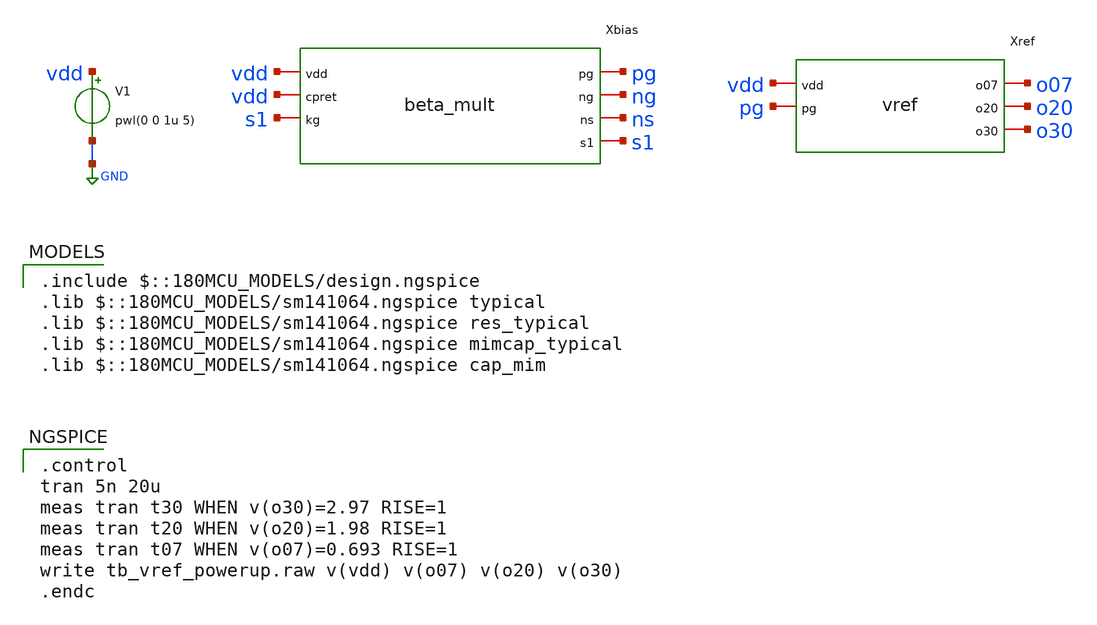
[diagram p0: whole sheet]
** sch_path: schematic pt2/sims/tb/tb_vref_powerup.sch
**.subckt tb_vref_powerup
V1 vdd GND pwl(0 0 1u 5)
Xbias vdd pg ng ns vdd s1 s1 beta_mult
Xref vdd pg o07 o20 o30 vref
**** begin user architecture code
 .include $::180MCU_MODELS/design.ngspice
.lib $::180MCU_MODELS/sm141064.ngspice typical
.lib $::180MCU_MODELS/sm141064.ngspice res_typical
.lib $::180MCU_MODELS/sm141064.ngspice mimcap_typical
.lib $::180MCU_MODELS/sm141064.ngspice cap_mim

.control
tran 5n 20u
meas tran t30 WHEN v(o30)=2.97 RISE=1
meas tran t20 WHEN v(o20)=1.98 RISE=1
meas tran t07 WHEN v(o07)=0.693 RISE=1
write tb_vref_powerup.raw v(vdd) v(o07) v(o20) v(o30)
.endc

**** end user architecture code
**.ends
.GLOBAL GND
.end
